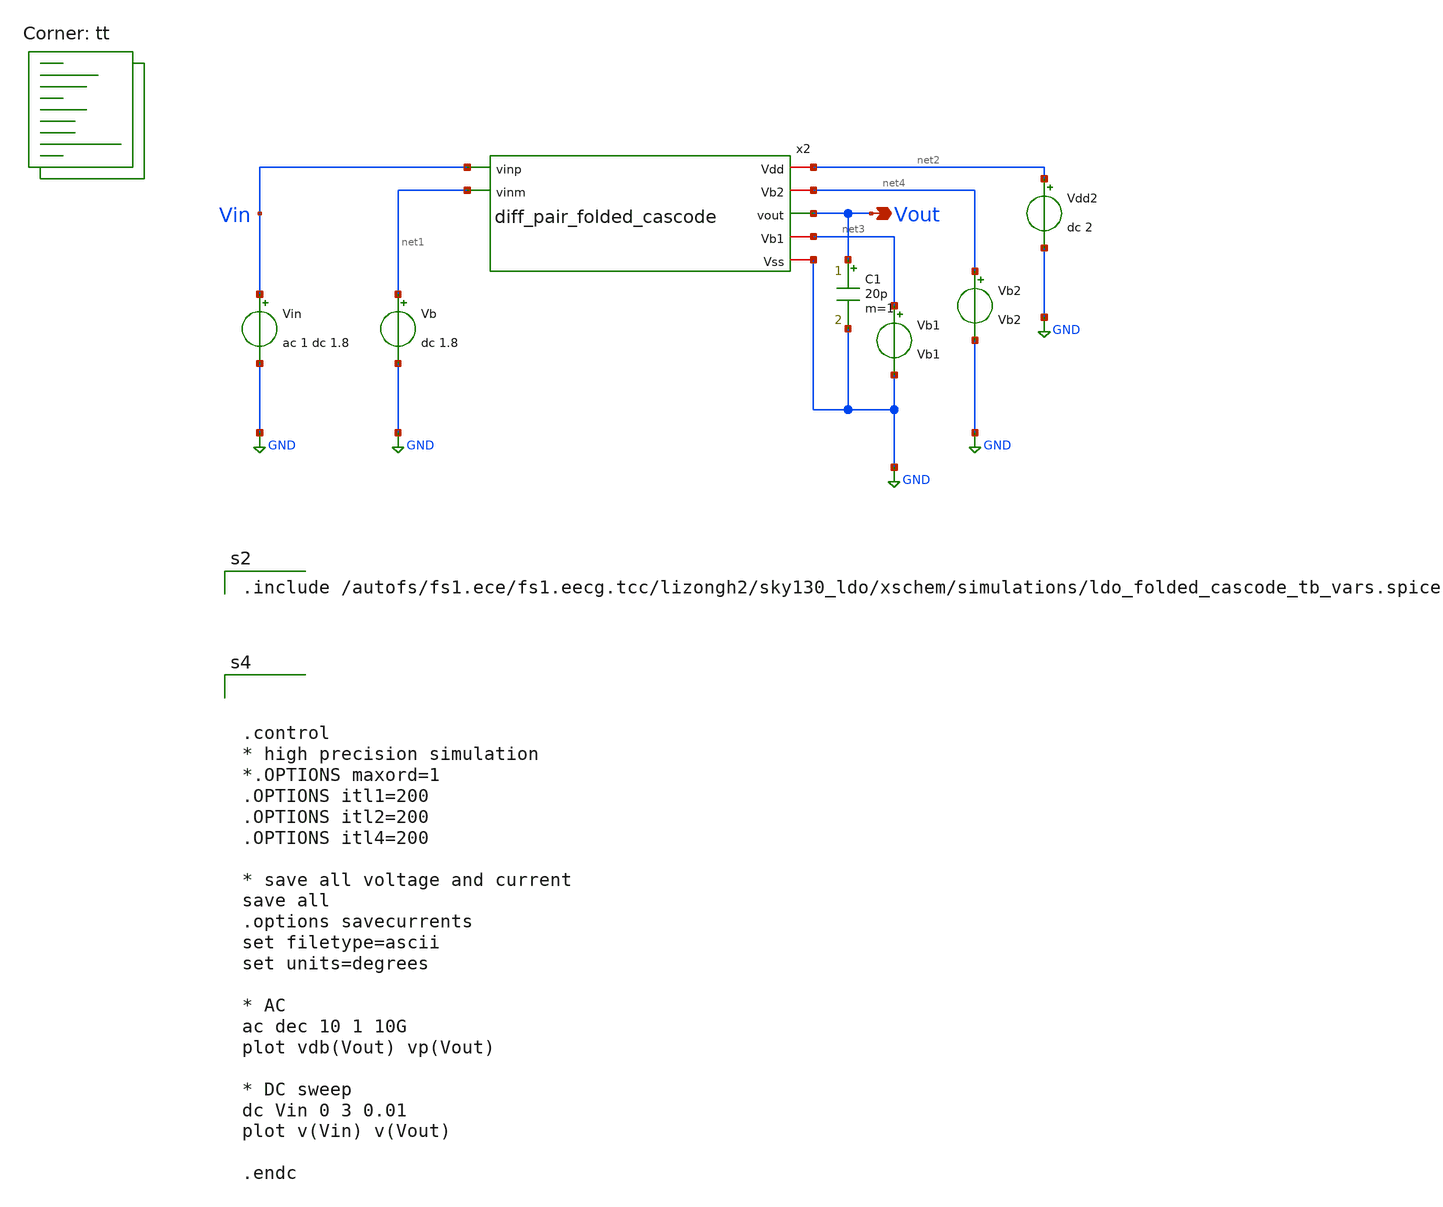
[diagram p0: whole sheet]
** sch_path: xschem/folded_cascode_tb.sch
**.subckt folded_cascode_tb Vout
*.opin Vout
x2 net2 net4 Vin net1 Vout net3 GND diff_pair_folded_cascode
Vin Vin GND ac 1 dc 1.8
Vb net1 GND dc 1.8
Vdd2 net2 GND dc 2
Vb2 net4 GND Vb2
Vb1 net3 GND Vb1
C1 Vout GND 20p m=1
**** begin user architecture code
.lib $::SKYWATER_MODELS/sky130.lib.spice tt

.include /autofs/fs1.ece/fs1.eecg.tcc/lizongh2/sky130_ldo/xschem/simulations/ldo_folded_cascode_tb_vars.spice





.control
* high precision simulation
*.OPTIONS maxord=1
.OPTIONS itl1=200
.OPTIONS itl2=200
.OPTIONS itl4=200

* save all voltage and current
save all
.options savecurrents
set filetype=ascii
set units=degrees

* AC
ac dec 10 1 10G
plot vdb(Vout) vp(Vout)

* DC sweep
dc Vin 0 3 0.01
plot v(Vin) v(Vout)

.endc


**** end user architecture code
**.ends

* expanding   symbol:  diff_pair_folded_cascode.sym # of pins=7
** sym_path: xschem/diff_pair_folded_cascode.sym
** sch_path: xschem/diff_pair_folded_cascode.sch
.subckt diff_pair_folded_cascode Vdd Vb2 vinp vinm vout Vb1 Vss
*.iopin Vdd
*.ipin vinm
*.ipin vinp
*.iopin Vb1
*.iopin Vss
*.iopin Vb2
*.opin vout
XM1 net2 vinp net4 Vss sky130_fd_pr__nfet_g5v0d10v5 L=L_M1 W=W_M1 nf=1 ad='int((nf+1)/2) * W/nf * 0.29'
+ as='int((nf+2)/2) * W/nf * 0.29' pd='2*int((nf+1)/2) * (W/nf + 0.29)' ps='2*int((nf+2)/2) * (W/nf + 0.29)'
+ nrd='0.29 / W' nrs='0.29 / W' sa=0 sb=0 sd=0 mult=1 m=1
XM2 net3 vinm net4 Vss sky130_fd_pr__nfet_g5v0d10v5 L=L_M2 W=W_M2 nf=1 ad='int((nf+1)/2) * W/nf * 0.29'
+ as='int((nf+2)/2) * W/nf * 0.29' pd='2*int((nf+1)/2) * (W/nf + 0.29)' ps='2*int((nf+2)/2) * (W/nf + 0.29)'
+ nrd='0.29 / W' nrs='0.29 / W' sa=0 sb=0 sd=0 mult=1 m=1
XM4 net3 net1 Vdd Vdd sky130_fd_pr__pfet_g5v0d10v5 L=L_M4 W=W_M4 nf=1 ad='int((nf+1)/2) * W/nf * 0.29'
+ as='int((nf+2)/2) * W/nf * 0.29' pd='2*int((nf+1)/2) * (W/nf + 0.29)' ps='2*int((nf+2)/2) * (W/nf + 0.29)'
+ nrd='0.29 / W' nrs='0.29 / W' sa=0 sb=0 sd=0 mult=1 m=1
XM3 net2 net1 Vdd Vdd sky130_fd_pr__pfet_g5v0d10v5 L=L_M3 W=W_M3 nf=1 ad='int((nf+1)/2) * W/nf * 0.29'
+ as='int((nf+2)/2) * W/nf * 0.29' pd='2*int((nf+1)/2) * (W/nf + 0.29)' ps='2*int((nf+2)/2) * (W/nf + 0.29)'
+ nrd='0.29 / W' nrs='0.29 / W' sa=0 sb=0 sd=0 mult=1 m=1
XM9 net4 Vb1 Vss Vss sky130_fd_pr__nfet_g5v0d10v5 L=L_M9 W=W_M9 nf=1 ad='int((nf+1)/2) * W/nf * 0.29'
+ as='int((nf+2)/2) * W/nf * 0.29' pd='2*int((nf+1)/2) * (W/nf + 0.29)' ps='2*int((nf+2)/2) * (W/nf + 0.29)'
+ nrd='0.29 / W' nrs='0.29 / W' sa=0 sb=0 sd=0 mult=1 m=1
XM6 vout Vb2 net3 Vdd sky130_fd_pr__pfet_g5v0d10v5 L=L_M6 W=W_M6 nf=1 ad='int((nf+1)/2) * W/nf * 0.29'
+ as='int((nf+2)/2) * W/nf * 0.29' pd='2*int((nf+1)/2) * (W/nf + 0.29)' ps='2*int((nf+2)/2) * (W/nf + 0.29)'
+ nrd='0.29 / W' nrs='0.29 / W' sa=0 sb=0 sd=0 mult=1 m=1
XM5 net1 Vb2 net2 Vdd sky130_fd_pr__pfet_g5v0d10v5 L=L_M5 W=W_M5 nf=1 ad='int((nf+1)/2) * W/nf * 0.29'
+ as='int((nf+2)/2) * W/nf * 0.29' pd='2*int((nf+1)/2) * (W/nf + 0.29)' ps='2*int((nf+2)/2) * (W/nf + 0.29)'
+ nrd='0.29 / W' nrs='0.29 / W' sa=0 sb=0 sd=0 mult=1 m=1
XM7 net1 Vb1 Vss Vss sky130_fd_pr__nfet_g5v0d10v5 L=L_M7 W=W_M7 nf=1 ad='int((nf+1)/2) * W/nf * 0.29'
+ as='int((nf+2)/2) * W/nf * 0.29' pd='2*int((nf+1)/2) * (W/nf + 0.29)' ps='2*int((nf+2)/2) * (W/nf + 0.29)'
+ nrd='0.29 / W' nrs='0.29 / W' sa=0 sb=0 sd=0 mult=1 m=1
XM8 vout Vb1 Vss Vss sky130_fd_pr__nfet_g5v0d10v5 L=L_M8 W=W_M8 nf=1 ad='int((nf+1)/2) * W/nf * 0.29'
+ as='int((nf+2)/2) * W/nf * 0.29' pd='2*int((nf+1)/2) * (W/nf + 0.29)' ps='2*int((nf+2)/2) * (W/nf + 0.29)'
+ nrd='0.29 / W' nrs='0.29 / W' sa=0 sb=0 sd=0 mult=1 m=1
.ends

.GLOBAL GND
.end
